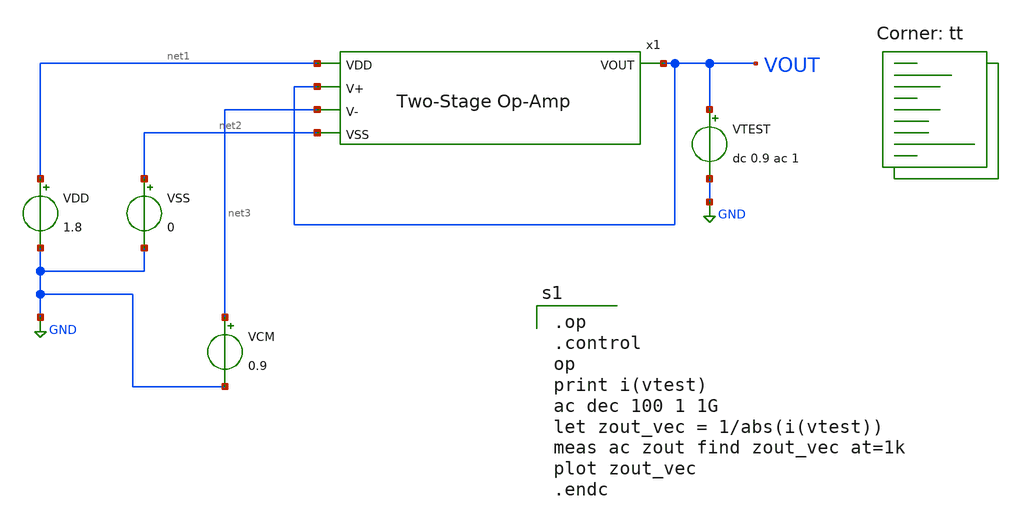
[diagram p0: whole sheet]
** sch_path: analog/schematics/tb_output_impedance.sch
**.subckt tb_output_impedance
x1 net1 VOUT net3 VOUT net2 bootcamp_opamp
VDD net1 GND 1.8
VSS net2 GND 0
VCM net3 GND 0.9
VTEST VOUT GND dc 0.9 ac 1
**** begin user architecture code

.op
.control
op
print i(vtest)
ac dec 100 1 1G
let zout_vec = 1/abs(i(vtest))
meas ac zout find zout_vec at=1k
plot zout_vec
.endc

.lib $::SKYWATER_MODELS/sky130.lib.spice tt
**** end user architecture code
**.ends

* expanding   symbol:  bootcamp_opamp.sym # of pins=5
** sym_path: analog/schematics/bootcamp_opamp.sym
** sch_path: analog/schematics/bootcamp_opamp.sch
.subckt bootcamp_opamp VDD V+ V- VOUT VSS
*.ipin V+
*.ipin V-
*.opin VOUT
*.ipin VDD
*.ipin VSS
XM1 net1 V+ net3 VSS sky130_fd_pr__nfet_01v8 L=1 W=4 nf=1 ad='int((nf+1)/2) * W/nf * 0.29' as='int((nf+2)/2) * W/nf * 0.29'
+ pd='2*int((nf+1)/2) * (W/nf + 0.29)' ps='2*int((nf+2)/2) * (W/nf + 0.29)' nrd='0.29 / W' nrs='0.29 / W'
+ sa=0 sb=0 sd=0 mult=1 m=1
XM2 net2 V- net3 VSS sky130_fd_pr__nfet_01v8 L=1 W=4 nf=1 ad='int((nf+1)/2) * W/nf * 0.29' as='int((nf+2)/2) * W/nf * 0.29'
+ pd='2*int((nf+1)/2) * (W/nf + 0.29)' ps='2*int((nf+2)/2) * (W/nf + 0.29)' nrd='0.29 / W' nrs='0.29 / W'
+ sa=0 sb=0 sd=0 mult=1 m=1
XM3 net1 net1 VDD VDD sky130_fd_pr__pfet_01v8 L=1 W=4 nf=1 ad='int((nf+1)/2) * W/nf * 0.29' as='int((nf+2)/2) * W/nf * 0.29'
+ pd='2*int((nf+1)/2) * (W/nf + 0.29)' ps='2*int((nf+2)/2) * (W/nf + 0.29)' nrd='0.29 / W' nrs='0.29 / W'
+ sa=0 sb=0 sd=0 mult=1 m=1
XM4 net2 net1 VDD VDD sky130_fd_pr__pfet_01v8 L=1 W=4 nf=1 ad='int((nf+1)/2) * W/nf * 0.29' as='int((nf+2)/2) * W/nf * 0.29'
+ pd='2*int((nf+1)/2) * (W/nf + 0.29)' ps='2*int((nf+2)/2) * (W/nf + 0.29)' nrd='0.29 / W' nrs='0.29 / W'
+ sa=0 sb=0 sd=0 mult=1 m=1
XM5 net3 net4 VSS VSS sky130_fd_pr__nfet_01v8 L=2 W=4 nf=1 ad='int((nf+1)/2) * W/nf * 0.29' as='int((nf+2)/2) * W/nf * 0.29'
+ pd='2*int((nf+1)/2) * (W/nf + 0.29)' ps='2*int((nf+2)/2) * (W/nf + 0.29)' nrd='0.29 / W' nrs='0.29 / W'
+ sa=0 sb=0 sd=0 mult=1 m=1
XM6 net4 net4 VSS VSS sky130_fd_pr__nfet_01v8 L=2 W=4 nf=1 ad='int((nf+1)/2) * W/nf * 0.29' as='int((nf+2)/2) * W/nf * 0.29'
+ pd='2*int((nf+1)/2) * (W/nf + 0.29)' ps='2*int((nf+2)/2) * (W/nf + 0.29)' nrd='0.29 / W' nrs='0.29 / W'
+ sa=0 sb=0 sd=0 mult=1 m=1
XM8 VOUT net4 VSS VSS sky130_fd_pr__nfet_01v8 L=0.5 W=2 nf=1 ad='int((nf+1)/2) * W/nf * 0.29' as='int((nf+2)/2) * W/nf * 0.29'
+ pd='2*int((nf+1)/2) * (W/nf + 0.29)' ps='2*int((nf+2)/2) * (W/nf + 0.29)' nrd='0.29 / W' nrs='0.29 / W'
+ sa=0 sb=0 sd=0 mult=1 m=1
XC1 net2 VOUT sky130_fd_pr__cap_mim_m3_1 W=22 L=22 MF=1 m=1
R1 VDD net4 12k m=1
XM7 VOUT net2 VDD VDD sky130_fd_pr__pfet_01v8 L=0.5 W=8 nf=1 ad='int((nf+1)/2) * W/nf * 0.29' as='int((nf+2)/2) * W/nf * 0.29'
+ pd='2*int((nf+1)/2) * (W/nf + 0.29)' ps='2*int((nf+2)/2) * (W/nf + 0.29)' nrd='0.29 / W' nrs='0.29 / W'
+ sa=0 sb=0 sd=0 mult=1 m=1
.ends

.GLOBAL GND
.end
